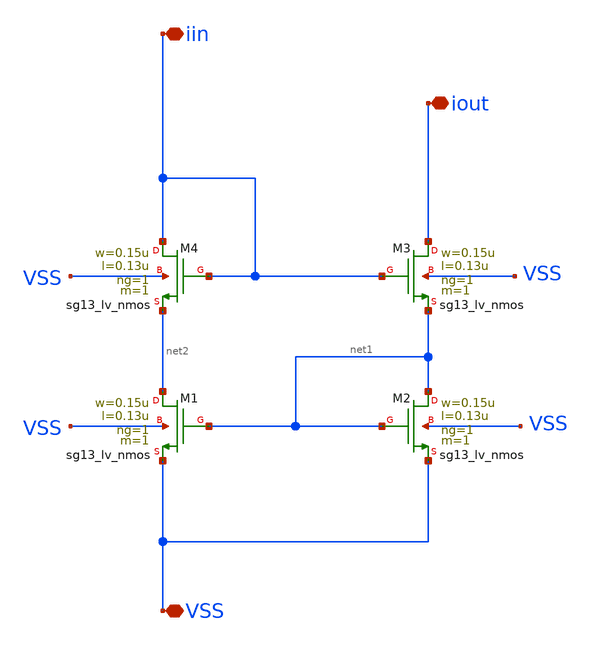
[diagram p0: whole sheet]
** sch_path: analog-db/templates/current_mirror/nmos_current_sink/improved_wilson_current_mirror.sch
* Copyright 2026 MacAnalog Research Group
**.subckt improved_wilson_current_mirror VSS iin iout
*.iopin VSS
*.iopin iin
*.iopin iout
XM1 net2 net1 VSS VSS sg13_lv_nmos w=0.15u l=0.13u ng=1 m=1 mm_ok=1
XM2 net1 net1 VSS VSS sg13_lv_nmos w=0.15u l=0.13u ng=1 m=1 mm_ok=1
XM3 iout iin net1 VSS sg13_lv_nmos w=0.15u l=0.13u ng=1 m=1 mm_ok=1
XM4 iin iin net2 VSS sg13_lv_nmos w=0.15u l=0.13u ng=1 m=1 mm_ok=1
**.ends
.end
